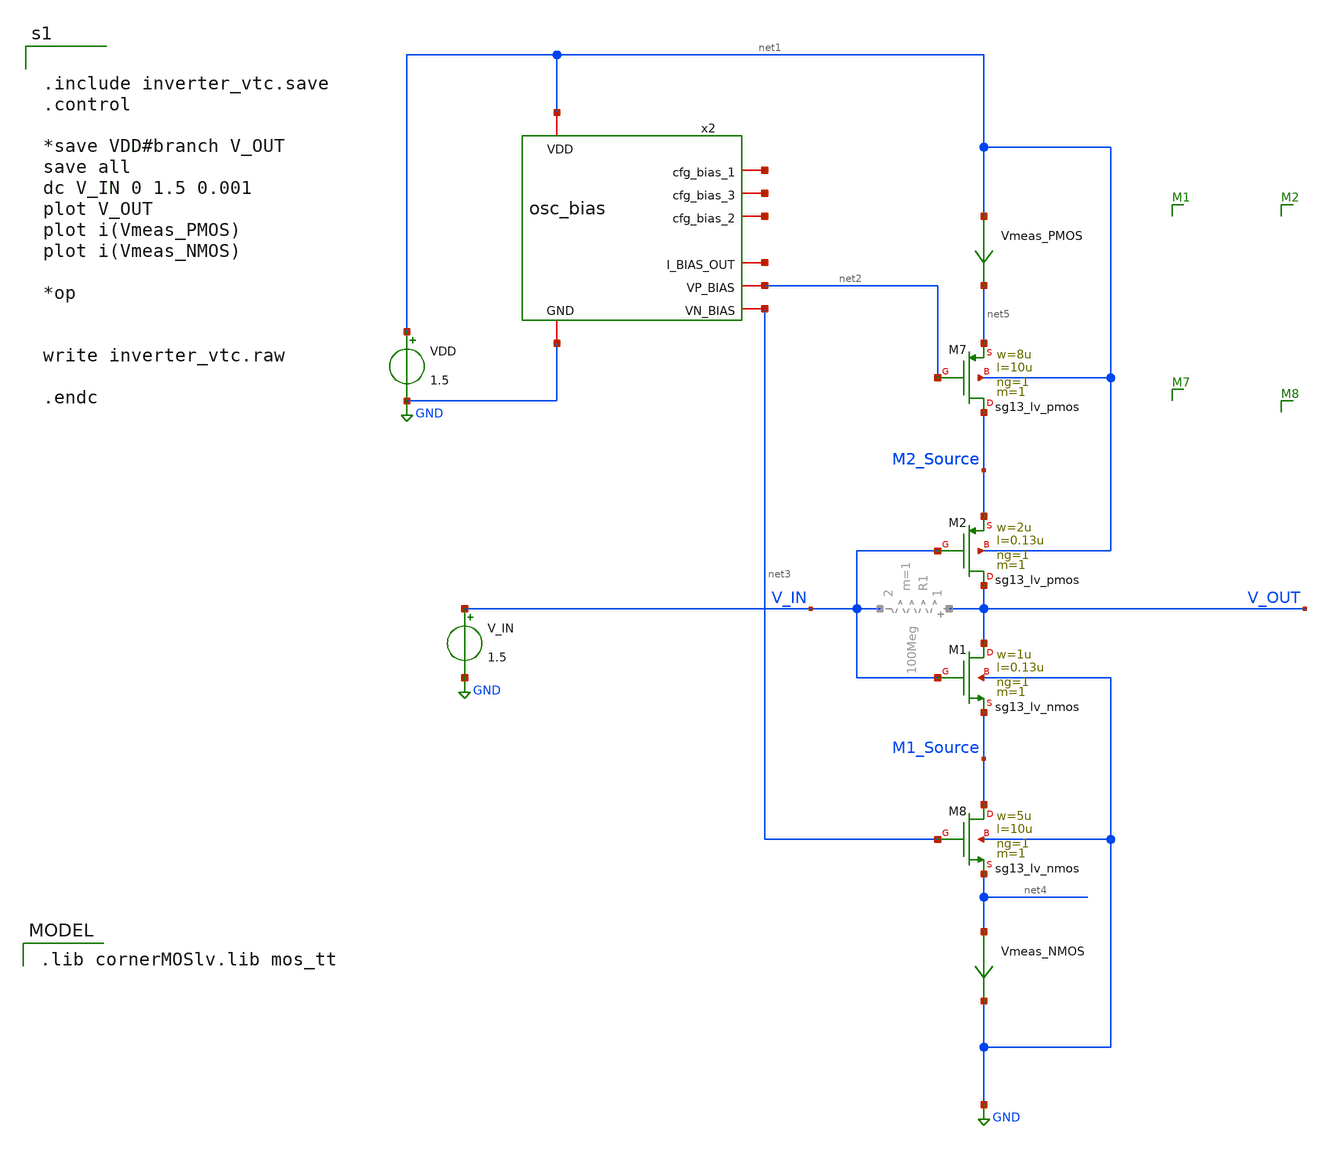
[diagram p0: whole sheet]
** sch_path: inverter_vtc.sch
**.subckt inverter_vtc
XM1 V_OUT V_IN M1_Source GND sg13_lv_nmos w=1u l=0.13u ng=1 m=1 mm_ok=1
XM2 V_OUT V_IN M2_Source net1 sg13_lv_pmos w=2u l=0.13u ng=1 m=1 mm_ok=1
Vmeas_NMOS net4 GND 0
.save i(vmeas_nmos)
Vmeas_PMOS net1 net5 0
.save i(vmeas_pmos)
VDD net1 GND 1.5
V_IN V_IN GND 1.5
x2 net1 net6 net7 net8 GND net9 net2 net3 osc_bias
XM7 M2_Source net2 net5 net1 sg13_lv_pmos w=8u l=10u ng=1 m=1 mm_ok=1
XM8 M1_Source net3 net4 GND sg13_lv_nmos w=5u l=10u ng=1 m=1 mm_ok=1
**** begin user architecture code
 .lib cornerMOSlv.lib mos_tt



.include inverter_vtc.save
.control

*save VDD#branch V_OUT
save all
dc V_IN 0 1.5 0.001
plot V_OUT
plot i(Vmeas_PMOS)
plot i(Vmeas_NMOS)

*op


write inverter_vtc.raw

.endc


**** end user architecture code
**.ends

* expanding   symbol:  osc_bias.sym # of pins=8
** sym_path: osc_bias.sym
** sch_path: osc_bias.sch
.subckt osc_bias VDD cfg_bias_1 cfg_bias_3 cfg_bias_2 GND I_BIAS_OUT VP_BIAS VN_BIAS
*.iopin VDD
*.iopin GND
*.iopin I_BIAS_OUT
*.iopin cfg_bias_1
*.iopin cfg_bias_2
*.iopin cfg_bias_3
*.opin VN_BIAS
*.opin VP_BIAS
XM1 VP_BIAS VP_BIAS VDD VDD sg13_lv_pmos w=1u l=10u ng=1 m=1 mm_ok=1
XM3 VP_BIAS VP_BIAS net1 VN_BIAS sg13_lv_nmos w=0.25u l=10u ng=1 m=1 mm_ok=1
XM4 net1 net1 net2 VN_BIAS sg13_lv_nmos w=0.25u l=10u ng=1 m=1 mm_ok=1
XM5 net2 net2 VN_BIAS VN_BIAS sg13_lv_nmos w=0.25u l=10u ng=1 m=1 mm_ok=1
XM2 net6 VP_BIAS VDD VDD sg13_lv_pmos w=0.5u l=10u ng=1 m=1 mm_ok=1
XM6 I_BIAS_OUT cfg_bias_1 net6 VDD sg13_lv_pmos w=0.5u l=5u ng=1 m=1 mm_ok=1
XM7 net3 VP_BIAS VDD VDD sg13_lv_pmos w=0.5u l=10u ng=1 m=1 mm_ok=1
XM8 net4 VP_BIAS VDD VDD sg13_lv_pmos w=0.5u l=10u ng=1 m=1 mm_ok=1
XM9 I_BIAS_OUT cfg_bias_2 net3 VDD sg13_lv_pmos w=0.5u l=10u ng=1 m=1 mm_ok=1
XM10 I_BIAS_OUT cfg_bias_3 net4 VDD sg13_lv_pmos w=0.5u l=10u ng=1 m=1 mm_ok=1
XM11 VN_BIAS VN_BIAS net5 VN_BIAS sg13_lv_nmos w=0.25u l=10u ng=1 m=1 mm_ok=1
Vmeas net5 GND 0
.save i(vmeas)
.ends

.GLOBAL GND
.end
